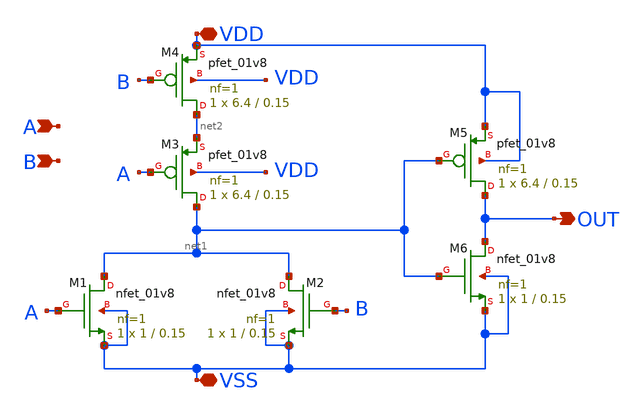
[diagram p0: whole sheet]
** sch_path: design/8_BIT_OR/xschem/or2.sch
**.subckt or2 A B VSS VDD OUT
*.ipin A
*.ipin B
*.iopin VSS
*.iopin VDD
*.opin OUT
XM3 net1 A net2 VDD sky130_fd_pr__pfet_01v8 L=0.15 W=6.4 nf=1 ad='int((nf+1)/2) * W/nf * 0.29' as='int((nf+2)/2) * W/nf * 0.29'
+ pd='2*int((nf+1)/2) * (W/nf + 0.29)' ps='2*int((nf+2)/2) * (W/nf + 0.29)' nrd='0.29 / W' nrs='0.29 / W'
+ sa=0 sb=0 sd=0 mult=1 m=1
XM4 net2 B VDD VDD sky130_fd_pr__pfet_01v8 L=0.15 W=6.4 nf=1 ad='int((nf+1)/2) * W/nf * 0.29' as='int((nf+2)/2) * W/nf * 0.29'
+ pd='2*int((nf+1)/2) * (W/nf + 0.29)' ps='2*int((nf+2)/2) * (W/nf + 0.29)' nrd='0.29 / W' nrs='0.29 / W'
+ sa=0 sb=0 sd=0 mult=1 m=1
XM1 net1 A VSS VSS sky130_fd_pr__nfet_01v8 L=0.15 W=1 nf=1 ad='int((nf+1)/2) * W/nf * 0.29' as='int((nf+2)/2) * W/nf * 0.29'
+ pd='2*int((nf+1)/2) * (W/nf + 0.29)' ps='2*int((nf+2)/2) * (W/nf + 0.29)' nrd='0.29 / W' nrs='0.29 / W'
+ sa=0 sb=0 sd=0 mult=1 m=1
XM2 net1 B VSS VSS sky130_fd_pr__nfet_01v8 L=0.15 W=1 nf=1 ad='int((nf+1)/2) * W/nf * 0.29' as='int((nf+2)/2) * W/nf * 0.29'
+ pd='2*int((nf+1)/2) * (W/nf + 0.29)' ps='2*int((nf+2)/2) * (W/nf + 0.29)' nrd='0.29 / W' nrs='0.29 / W'
+ sa=0 sb=0 sd=0 mult=1 m=1
XM5 OUT net1 VDD VDD sky130_fd_pr__pfet_01v8 L=0.15 W=6.4 nf=1 ad='int((nf+1)/2) * W/nf * 0.29' as='int((nf+2)/2) * W/nf * 0.29'
+ pd='2*int((nf+1)/2) * (W/nf + 0.29)' ps='2*int((nf+2)/2) * (W/nf + 0.29)' nrd='0.29 / W' nrs='0.29 / W'
+ sa=0 sb=0 sd=0 mult=1 m=1
XM6 OUT net1 VSS VSS sky130_fd_pr__nfet_01v8 L=0.15 W=1 nf=1 ad='int((nf+1)/2) * W/nf * 0.29' as='int((nf+2)/2) * W/nf * 0.29'
+ pd='2*int((nf+1)/2) * (W/nf + 0.29)' ps='2*int((nf+2)/2) * (W/nf + 0.29)' nrd='0.29 / W' nrs='0.29 / W'
+ sa=0 sb=0 sd=0 mult=1 m=1
**.ends
.end
